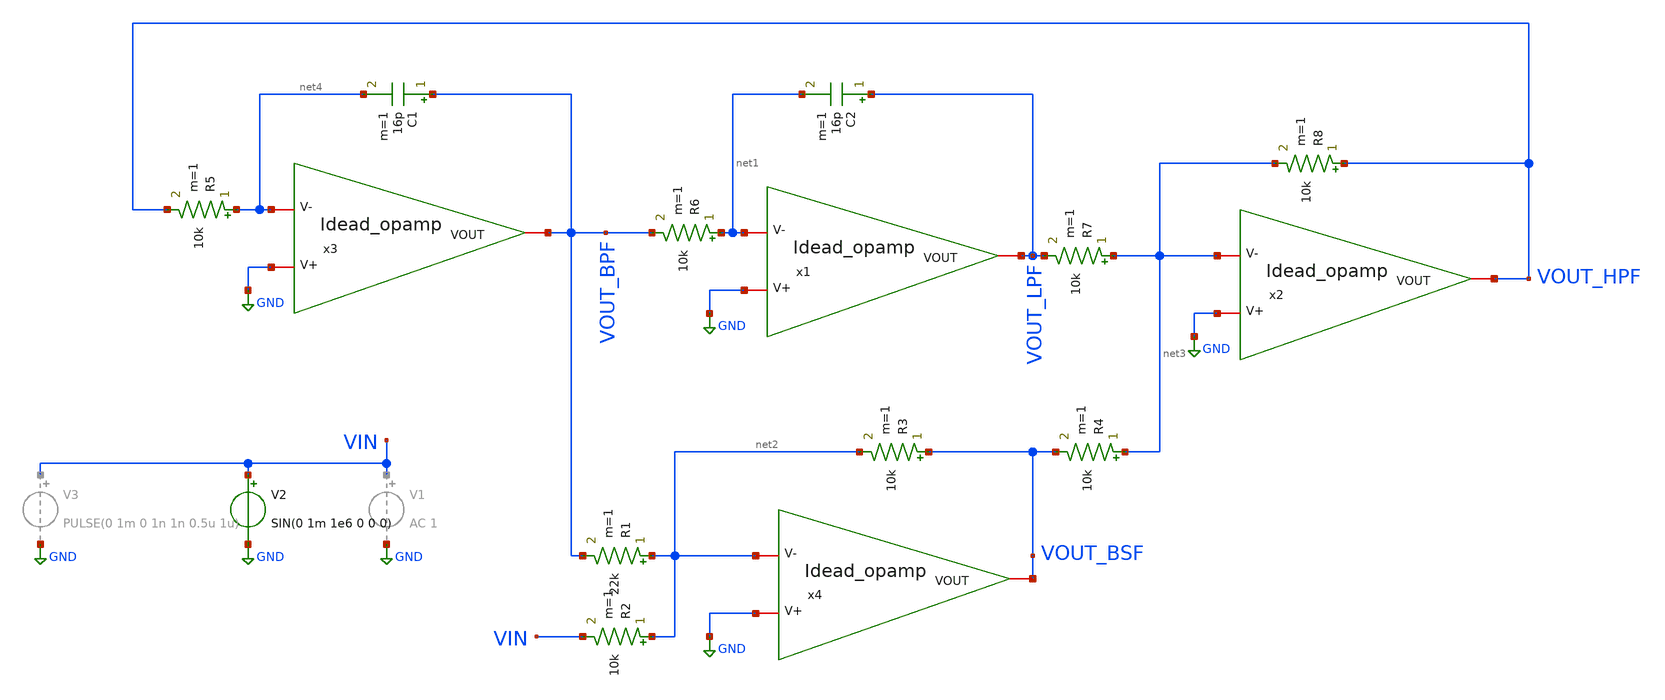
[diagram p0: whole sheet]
** sch_path: Design/Testbench.sch
**.subckt Testbench
x1 VOUT_LPF net1 GND Idead_opamp
x2 VOUT_HPF net3 GND Idead_opamp
x3 VOUT_BPF net4 GND Idead_opamp
x4 VOUT_BSF net2 GND Idead_opamp
R1 net2 VOUT_BPF 22k m=1
C1 VOUT_BPF net4 16p m=1
R2 net2 VIN 10k m=1
R3 VOUT_BSF net2 10k m=1
R4 net3 VOUT_BSF 10k m=1
R5 net4 VOUT_HPF 10k m=1
R6 net1 VOUT_BPF 10k m=1
R7 net3 VOUT_LPF 10k m=1
R8 VOUT_HPF net3 10k m=1
C2 VOUT_LPF net1 16p m=1
V2 VIN GND SIN(0 1m 1e6 0 0 0)
**** begin user architecture code

.include sim_script_tran.sim

**** end user architecture code
**.ends

* expanding   symbol:  Idead_opamp.sym # of pins=3
** sym_path: Design/Idead_opamp.sym
** sch_path: Design/Idead_opamp.sch
.subckt Idead_opamp VOUT V- V+
*.iopin V-
*.iopin V+
*.iopin VOUT
E1 VOUT GND V+ V- 10000
.ends

.GLOBAL GND
.end
